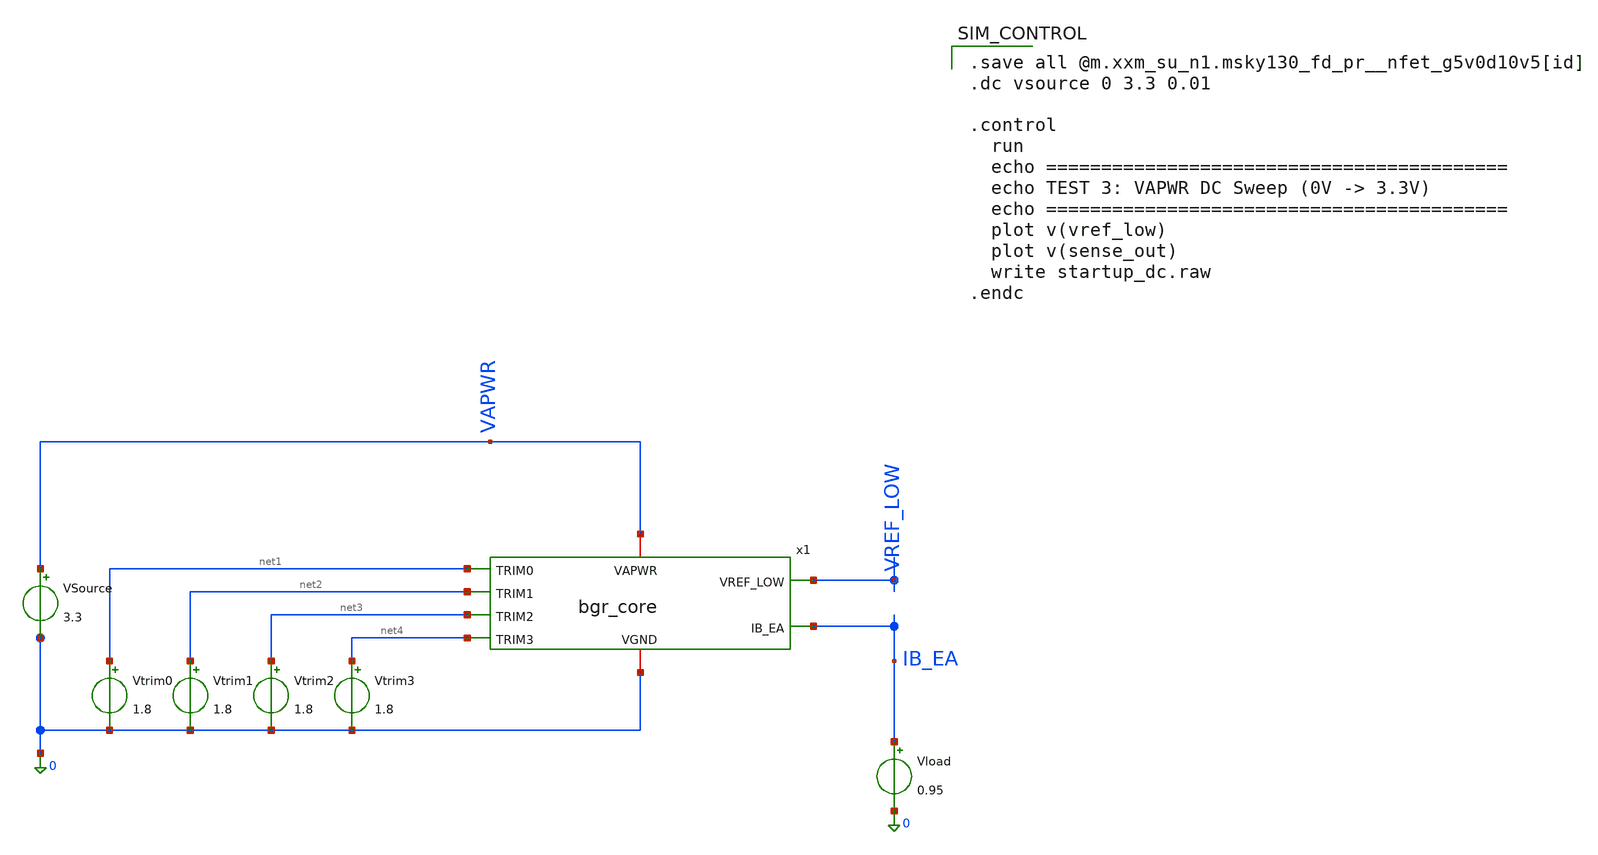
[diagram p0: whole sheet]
** sch_path: designs/bgr_ldo/bgr/bgr_core_tb2.sch
**.subckt bgr_core_tb2
VSource VAPWR 0 3.3
Vload IB_EA 0 0.95
Vtrim0 net1 0 1.8
Vtrim1 net2 0 1.8
Vtrim2 net3 0 1.8
Vtrim3 net4 0 1.8
x1 VAPWR VREF_LOW IB_EA net1 net2 net3 net4 0 bgr_core
**** begin user architecture code

.save all @m.xxm_su_n1.msky130_fd_pr__nfet_g5v0d10v5[id]
.dc vsource 0 3.3 0.01

.control
  run
  echo ==========================================
  echo TEST 3: VAPWR DC Sweep (0V -> 3.3V)
  echo ==========================================
  plot v(vref_low)
  plot v(sense_out)
  write startup_dc.raw
.endc


** opencircuitdesign pdks install
.lib $::SKYWATER_MODELS/sky130.lib.spice tt

**** end user architecture code
**.ends

* expanding   symbol:  bgr_core.sym # of pins=8
** sym_path: designs/bgr_ldo/bgr/bgr_core.sym
** sch_path: designs/bgr_ldo/bgr/bgr_core.sch
.subckt bgr_core VAPWR VREF_LOW IB_EA TRIM0 TRIM1 TRIM2 TRIM3 VGND
*.iopin VAPWR
*.opin VREF_LOW
*.iopin VGND
*.opin IB_EA
*.ipin TRIM0
*.ipin TRIM1
*.ipin TRIM2
*.ipin TRIM3
XXQA VGND VGND VBE1 sky130_fd_pr__pnp_05v5_W0p68L0p68 m=1
XXQB VGND VGND VBE8 sky130_fd_pr__pnp_05v5_W0p68L0p68 m=8
XXM_top1 net2 V_gate_top VAPWR VAPWR sky130_fd_pr__pfet_g5v0d10v5 L=4 W=20 nf=1 ad='int((1 + 1)/2) * 20 / 1 * 0.29'
+ as='int((1 + 2)/2) * 20 / 1 * 0.29' pd='2*int((1 + 1)/2) * (20 / 1 + 0.29)' ps='2*int((1 + 2)/2) * (20 / 1 + 0.29)'
+ nrd='0.29 / 20 ' nrs='0.29 / 20 ' sa=0 sb=0 sd=0 mult=4 m=4
XXM_top2 net3 V_gate_top VAPWR VAPWR sky130_fd_pr__pfet_g5v0d10v5 L=4 W=20 nf=1 ad='int((1 + 1)/2) * 20 / 1 * 0.29'
+ as='int((1 + 2)/2) * 20 / 1 * 0.29' pd='2*int((1 + 1)/2) * (20 / 1 + 0.29)' ps='2*int((1 + 2)/2) * (20 / 1 + 0.29)'
+ nrd='0.29 / 20 ' nrs='0.29 / 20 ' sa=0 sb=0 sd=0 mult=4 m=4
XXM_top5 net6 V_gate_top VAPWR VAPWR sky130_fd_pr__pfet_g5v0d10v5 L=4 W=20 nf=1 ad='int((1 + 1)/2) * 20 / 1 * 0.29'
+ as='int((1 + 2)/2) * 20 / 1 * 0.29' pd='2*int((1 + 1)/2) * (20 / 1 + 0.29)' ps='2*int((1 + 2)/2) * (20 / 1 + 0.29)'
+ nrd='0.29 / 20 ' nrs='0.29 / 20 ' sa=0 sb=0 sd=0 mult=4 m=4
XXM3 net4 V_mid1 VBE1 VGND sky130_fd_pr__nfet_g5v0d10v5 L=4 W=20 nf=1 ad='int((1 + 1)/2) * 20 / 1 * 0.29'
+ as='int((1 + 2)/2) * 20 / 1 * 0.29' pd='2*int((1 + 1)/2) * (20 / 1 + 0.29)' ps='2*int((1 + 2)/2) * (20 / 1 + 0.29)'
+ nrd='0.29 / 20 ' nrs='0.29 / 20 ' sa=0 sb=0 sd=0 mult=2 m=2
XXM4 net5 V_mid1 net1 VGND sky130_fd_pr__nfet_g5v0d10v5 L=4 W=20 nf=1 ad='int((1 + 1)/2) * 20 / 1 * 0.29'
+ as='int((1 + 2)/2) * 20 / 1 * 0.29' pd='2*int((1 + 1)/2) * (20 / 1 + 0.29)' ps='2*int((1 + 2)/2) * (20 / 1 + 0.29)'
+ nrd='0.29 / 20 ' nrs='0.29 / 20 ' sa=0 sb=0 sd=0 mult=2 m=2
XXM_bot1 V_mid1 V_bias net2 VAPWR sky130_fd_pr__pfet_g5v0d10v5 L=2 W=10 nf=1 ad='int((1 + 1)/2) * 10 / 1 * 0.29'
+ as='int((1 + 2)/2) * 10 / 1 * 0.29' pd='2*int((1 + 1)/2) * (10 / 1 + 0.29)' ps='2*int((1 + 2)/2) * (10 / 1 + 0.29)'
+ nrd='0.29 / 10 ' nrs='0.29 / 10 ' sa=0 sb=0 sd=0 mult=4 m=4
XXM_bot2 V_gate_top V_bias net3 VAPWR sky130_fd_pr__pfet_g5v0d10v5 L=2 W=10 nf=1 ad='int((1 + 1)/2) * 10 / 1 * 0.29'
+ as='int((1 + 2)/2) * 10 / 1 * 0.29' pd='2*int((1 + 1)/2) * (10 / 1 + 0.29)' ps='2*int((1 + 2)/2) * (10 / 1 + 0.29)'
+ nrd='0.29 / 10 ' nrs='0.29 / 10 ' sa=0 sb=0 sd=0 mult=4 m=4
XXM_bot5 VREF_LOW V_bias net6 VAPWR sky130_fd_pr__pfet_g5v0d10v5 L=2 W=10 nf=1 ad='int((1 + 1)/2) * 10 / 1 * 0.29'
+ as='int((1 + 2)/2) * 10 / 1 * 0.29' pd='2*int((1 + 1)/2) * (10 / 1 + 0.29)' ps='2*int((1 + 2)/2) * (10 / 1 + 0.29)'
+ nrd='0.29 / 10 ' nrs='0.29 / 10 ' sa=0 sb=0 sd=0 mult=4 m=4
XXM_bias V_bias V_bias VAPWR VAPWR sky130_fd_pr__pfet_g5v0d10v5 L=4 W=10 nf=1 ad='int((1 + 1)/2) * 10 / 1 * 0.29'
+ as='int((1 + 2)/2) * 10 / 1 * 0.29' pd='2*int((1 + 1)/2) * (10 / 1 + 0.29)' ps='2*int((1 + 2)/2) * (10 / 1 + 0.29)'
+ nrd='0.29 / 10 ' nrs='0.29 / 10 ' sa=0 sb=0 sd=0 mult=1 m=1
XXM_bias_mir V_bias_n V_gate_top VAPWR VAPWR sky130_fd_pr__pfet_g5v0d10v5 L=2 W=10 nf=1 ad='int((1 + 1)/2) * 10 / 1 * 0.29'
+ as='int((1 + 2)/2) * 10 / 1 * 0.29' pd='2*int((1 + 1)/2) * (10 / 1 + 0.29)' ps='2*int((1 + 2)/2) * (10 / 1 + 0.29)'
+ nrd='0.29 / 10 ' nrs='0.29 / 10 ' sa=0 sb=0 sd=0 mult=4 m=4
XXM_bias_n1 V_bias_n V_bias_n VGND VGND sky130_fd_pr__nfet_g5v0d10v5 L=2 W=10 nf=1 ad='int((1 + 1)/2) * 10 / 1 * 0.29'
+ as='int((1 + 2)/2) * 10 / 1 * 0.29' pd='2*int((1 + 1)/2) * (10 / 1 + 0.29)' ps='2*int((1 + 2)/2) * (10 / 1 + 0.29)'
+ nrd='0.29 / 10 ' nrs='0.29 / 10 ' sa=0 sb=0 sd=0 mult=2 m=2
XXM_bias_n2 V_bias V_bias_n VGND VGND sky130_fd_pr__nfet_g5v0d10v5 L=2 W=10 nf=1 ad='int((1 + 1)/2) * 10 / 1 * 0.29'
+ as='int((1 + 2)/2) * 10 / 1 * 0.29' pd='2*int((1 + 1)/2) * (10 / 1 + 0.29)' ps='2*int((1 + 2)/2) * (10 / 1 + 0.29)'
+ nrd='0.29 / 10 ' nrs='0.29 / 10 ' sa=0 sb=0 sd=0 mult=2 m=2
XXM_su_n1 V_gate_top sense_out V_su_mid VGND sky130_fd_pr__nfet_g5v0d10v5 L=2 W=1 nf=1 ad='int((1 + 1)/2) * 1 / 1 * 0.29'
+ as='int((1 + 2)/2) * 1 / 1 * 0.29' pd='2*int((1 + 1)/2) * (1 / 1 + 0.29)' ps='2*int((1 + 2)/2) * (1 / 1 + 0.29)'
+ nrd='0.29 / 1 ' nrs='0.29 / 1 ' sa=0 sb=0 sd=0 mult=1 m=1
XXM_su_n2 V_su_mid V_su_mid VGND VGND sky130_fd_pr__nfet_g5v0d10v5 L=20 W=1 nf=1 ad='int((1 + 1)/2) * 1 / 1 * 0.29'
+ as='int((1 + 2)/2) * 1 / 1 * 0.29' pd='2*int((1 + 1)/2) * (1 / 1 + 0.29)' ps='2*int((1 + 2)/2) * (1 / 1 + 0.29)'
+ nrd='0.29 / 1 ' nrs='0.29 / 1 ' sa=0 sb=0 sd=0 mult=1 m=1
XXM_pd sense_out VBE1 VGND VGND sky130_fd_pr__nfet_g5v0d10v5 L=2 W=12 nf=1 ad='int((1 + 1)/2) * 12 / 1 * 0.29'
+ as='int((1 + 2)/2) * 12 / 1 * 0.29' pd='2*int((1 + 1)/2) * (12 / 1 + 0.29)' ps='2*int((1 + 2)/2) * (12 / 1 + 0.29)'
+ nrd='0.29 / 12 ' nrs='0.29 / 12 ' sa=0 sb=0 sd=0 mult=1 m=1
XXM_su1a sense_out V_bias_n net8 VAPWR sky130_fd_pr__pfet_g5v0d10v5 L=20 W=0.42 nf=1 ad='int((1 + 1)/2) * 0.42 / 1 * 0.29'
+ as='int((1 + 2)/2) * 0.42 / 1 * 0.29' pd='2*int((1 + 1)/2) * (0.42 / 1 + 0.29)' ps='2*int((1 + 2)/2) * (0.42 / 1 + 0.29)'
+ nrd='0.29 / 0.42 ' nrs='0.29 / 0.42 ' sa=0 sb=0 sd=0 mult=1 m=1
XXM_su1b net8 V_bias_n net7 VAPWR sky130_fd_pr__pfet_g5v0d10v5 L=20 W=0.42 nf=1 ad='int((1 + 1)/2) * 0.42 / 1 * 0.29'
+ as='int((1 + 2)/2) * 0.42 / 1 * 0.29' pd='2*int((1 + 1)/2) * (0.42 / 1 + 0.29)' ps='2*int((1 + 2)/2) * (0.42 / 1 + 0.29)'
+ nrd='0.29 / 0.42 ' nrs='0.29 / 0.42 ' sa=0 sb=0 sd=0 mult=1 m=1
XXM_su1c net7 V_bias_n VAPWR VAPWR sky130_fd_pr__pfet_g5v0d10v5 L=20 W=0.42 nf=1 ad='int((1 + 1)/2) * 0.42 / 1 * 0.29'
+ as='int((1 + 2)/2) * 0.42 / 1 * 0.29' pd='2*int((1 + 1)/2) * (0.42 / 1 + 0.29)' ps='2*int((1 + 2)/2) * (0.42 / 1 + 0.29)'
+ nrd='0.29 / 0.42 ' nrs='0.29 / 0.42 ' sa=0 sb=0 sd=0 mult=1 m=1
XR1 VBE8 net1 VGND sky130_fd_pr__res_high_po_0p69 L=34.29 mult=1 m=1
XR6_1 n_r6m VBE1 VGND sky130_fd_pr__res_high_po_0p69 L=121.730 mult=1 m=1
XR7_1 n_r7m net1 VGND sky130_fd_pr__res_high_po_0p69 L=121.730 mult=1 m=1
XR2fix n_b0 VREF_LOW VGND sky130_fd_pr__res_high_po_0p69 L=229.410 mult=1 m=1
XXM3c V_mid1 V_casc_n net4 VGND sky130_fd_pr__nfet_g5v0d10v5 L=2 W=10 nf=1 ad='int((1 + 1)/2) * 10 / 1 * 0.29'
+ as='int((1 + 2)/2) * 10 / 1 * 0.29' pd='2*int((1 + 1)/2) * (10 / 1 + 0.29)' ps='2*int((1 + 2)/2) * (10 / 1 + 0.29)'
+ nrd='0.29 / 10 ' nrs='0.29 / 10 ' sa=0 sb=0 sd=0 mult=2 m=2
XXM4c V_gate_top V_casc_n net5 VGND sky130_fd_pr__nfet_g5v0d10v5 L=2 W=10 nf=1 ad='int((1 + 1)/2) * 10 / 1 * 0.29'
+ as='int((1 + 2)/2) * 10 / 1 * 0.29' pd='2*int((1 + 1)/2) * (10 / 1 + 0.29)' ps='2*int((1 + 2)/2) * (10 / 1 + 0.29)'
+ nrd='0.29 / 10 ' nrs='0.29 / 10 ' sa=0 sb=0 sd=0 mult=2 m=2
XXM_cn_mir V_casc_n V_gate_top VAPWR VAPWR sky130_fd_pr__pfet_g5v0d10v5 L=2 W=10 nf=1 ad='int((1 + 1)/2) * 10 / 1 * 0.29'
+ as='int((1 + 2)/2) * 10 / 1 * 0.29' pd='2*int((1 + 1)/2) * (10 / 1 + 0.29)' ps='2*int((1 + 2)/2) * (10 / 1 + 0.29)'
+ nrd='0.29 / 10 ' nrs='0.29 / 10 ' sa=0 sb=0 sd=0 mult=1 m=1
XXM_cn_d2 V_casc_n V_casc_n cn_mid VGND sky130_fd_pr__nfet_g5v0d10v5 L=2 W=2 nf=1 ad='int((1 + 1)/2) * 2 / 1 * 0.29'
+ as='int((1 + 2)/2) * 2 / 1 * 0.29' pd='2*int((1 + 1)/2) * (2 / 1 + 0.29)' ps='2*int((1 + 2)/2) * (2 / 1 + 0.29)'
+ nrd='0.29 / 2 ' nrs='0.29 / 2 ' sa=0 sb=0 sd=0 mult=1 m=1
XXM_cn_d1 cn_mid cn_mid net9 VGND sky130_fd_pr__nfet_g5v0d10v5 L=2 W=2 nf=1 ad='int((1 + 1)/2) * 2 / 1 * 0.29'
+ as='int((1 + 2)/2) * 2 / 1 * 0.29' pd='2*int((1 + 1)/2) * (2 / 1 + 0.29)' ps='2*int((1 + 2)/2) * (2 / 1 + 0.29)'
+ nrd='0.29 / 2 ' nrs='0.29 / 2 ' sa=0 sb=0 sd=0 mult=1 m=1
XR_cn VGND net9 VGND sky130_fd_pr__res_high_po_0p69 L=91.205 mult=1 m=1
XXM_tap_top net_tap V_gate_top VAPWR VAPWR sky130_fd_pr__pfet_g5v0d10v5 L=4 W=20 nf=1 ad='int((1 + 1)/2) * 20 / 1 * 0.29'
+ as='int((1 + 2)/2) * 20 / 1 * 0.29' pd='2*int((1 + 1)/2) * (20 / 1 + 0.29)' ps='2*int((1 + 2)/2) * (20 / 1 + 0.29)'
+ nrd='0.29 / 20 ' nrs='0.29 / 20 ' sa=0 sb=0 sd=0 mult=1 m=1
XXM_tap_casc IB_EA V_bias net_tap VAPWR sky130_fd_pr__pfet_g5v0d10v5 L=2 W=10 nf=1 ad='int((1 + 1)/2) * 10 / 1 * 0.29'
+ as='int((1 + 2)/2) * 10 / 1 * 0.29' pd='2*int((1 + 1)/2) * (10 / 1 + 0.29)' ps='2*int((1 + 2)/2) * (10 / 1 + 0.29)'
+ nrd='0.29 / 10 ' nrs='0.29 / 10 ' sa=0 sb=0 sd=0 mult=1 m=1
XR2b0 n_b1 n_b0 VGND sky130_fd_pr__res_high_po_0p69 L=1.27 mult=1 m=1
XR2b1 n_b2 n_b1 VGND sky130_fd_pr__res_high_po_0p69 L=3.650 mult=1 m=1
XR2b2 n_b3 n_b2 VGND sky130_fd_pr__res_high_po_0p69 L=8.42 mult=1 m=1
XR2b3 VGND n_b3 VGND sky130_fd_pr__res_high_po_0p69 L=17.96 mult=1 m=1
x1 VGND n_b1 n_b0 n_b3 n_b2 TRIM0 TRIM1 TRIM3 TRIM2 VGND n_b3 n_b2 n_b1 trim_sw
XR6_2 VGND n_r6m VGND sky130_fd_pr__res_high_po_0p69 L=121.730 mult=1 m=1
XR7_2 VGND n_r7m VGND sky130_fd_pr__res_high_po_0p69 L=121.730 mult=1 m=1
XXDUM_B1 VAPWR VAPWR VAPWR VAPWR sky130_fd_pr__pfet_g5v0d10v5 L=2 W=10 nf=1 ad='int((1 + 1)/2) * 10 / 1 * 0.29'
+ as='int((1 + 2)/2) * 10 / 1 * 0.29' pd='2*int((1 + 1)/2) * (10 / 1 + 0.29)' ps='2*int((1 + 2)/2) * (10 / 1 + 0.29)'
+ nrd='0.29 / 10 ' nrs='0.29 / 10 ' sa=0 sb=0 sd=0 mult=1 m=1
XXDUM_B2 VAPWR VAPWR VAPWR VAPWR sky130_fd_pr__pfet_g5v0d10v5 L=2 W=10 nf=1 ad='int((1 + 1)/2) * 10 / 1 * 0.29'
+ as='int((1 + 2)/2) * 10 / 1 * 0.29' pd='2*int((1 + 1)/2) * (10 / 1 + 0.29)' ps='2*int((1 + 2)/2) * (10 / 1 + 0.29)'
+ nrd='0.29 / 10 ' nrs='0.29 / 10 ' sa=0 sb=0 sd=0 mult=1 m=1
XXDUM_C1 VGND VGND VGND VGND sky130_fd_pr__nfet_g5v0d10v5 L=4 W=20 nf=1 ad='int((1 + 1)/2) * 20 / 1 * 0.29'
+ as='int((1 + 2)/2) * 20 / 1 * 0.29' pd='2*int((1 + 1)/2) * (20 / 1 + 0.29)' ps='2*int((1 + 2)/2) * (20 / 1 + 0.29)'
+ nrd='0.29 / 20 ' nrs='0.29 / 20 ' sa=0 sb=0 sd=0 mult=1 m=1
XXDUM_C2 VGND VGND VGND VGND sky130_fd_pr__nfet_g5v0d10v5 L=4 W=20 nf=1 ad='int((1 + 1)/2) * 20 / 1 * 0.29'
+ as='int((1 + 2)/2) * 20 / 1 * 0.29' pd='2*int((1 + 1)/2) * (20 / 1 + 0.29)' ps='2*int((1 + 2)/2) * (20 / 1 + 0.29)'
+ nrd='0.29 / 20 ' nrs='0.29 / 20 ' sa=0 sb=0 sd=0 mult=1 m=1
XXDUM_D1 VGND VGND VGND VGND sky130_fd_pr__nfet_g5v0d10v5 L=2 W=10 nf=1 ad='int((1 + 1)/2) * 10 / 1 * 0.29'
+ as='int((1 + 2)/2) * 10 / 1 * 0.29' pd='2*int((1 + 1)/2) * (10 / 1 + 0.29)' ps='2*int((1 + 2)/2) * (10 / 1 + 0.29)'
+ nrd='0.29 / 10 ' nrs='0.29 / 10 ' sa=0 sb=0 sd=0 mult=1 m=1
XXDUM_D2 VGND VGND VGND VGND sky130_fd_pr__nfet_g5v0d10v5 L=2 W=10 nf=1 ad='int((1 + 1)/2) * 10 / 1 * 0.29'
+ as='int((1 + 2)/2) * 10 / 1 * 0.29' pd='2*int((1 + 1)/2) * (10 / 1 + 0.29)' ps='2*int((1 + 2)/2) * (10 / 1 + 0.29)'
+ nrd='0.29 / 10 ' nrs='0.29 / 10 ' sa=0 sb=0 sd=0 mult=1 m=1
XXDUM_Qn VGND VGND VGND sky130_fd_pr__pnp_05v5_W0p68L0p68 m=16
XXDUM_RA1 VGND VGND VGND sky130_fd_pr__res_high_po_0p69 L=31.49 mult=1 m=1
XXDUM_RA2 VGND VGND VGND sky130_fd_pr__res_high_po_0p69 L=31.49 mult=1 m=1
XXDUM_RB1 VGND VGND VGND sky130_fd_pr__res_high_po_0p69 L=58.41 mult=1 m=1
XXDUM_RB2 VGND VGND VGND sky130_fd_pr__res_high_po_0p69 L=58.41 mult=1 m=1
.ends


* expanding   symbol:  trim_sw.sym # of pins=13
** sym_path: designs/bgr_ldo/bgr/trim_sw.sym
** sch_path: designs/bgr_ldo/bgr/trim_sw.sch
.subckt trim_sw VGND SEG1A SEG0A SEG3A SEG2A TRIM0 TRIM1 TRIM3 TRIM2 SEG3B SEG2B SEG1B SEG0B
*.ipin TRIM0
*.ipin TRIM1
*.ipin TRIM2
*.ipin TRIM3
*.iopin SEG0A
*.iopin SEG0B
*.iopin SEG1A
*.iopin SEG2A
*.iopin SEG3A
*.iopin SEG1B
*.iopin SEG2B
*.iopin SEG3B
*.iopin VGND
XSWb0 SEG0A TRIM0 SEG0B VGND sky130_fd_pr__nfet_01v8 L=0.15 W=10 nf=1 ad='int((1 + 1)/2) * 10 / 1 * 0.29'
+ as='int((1 + 2)/2) * 10 / 1 * 0.29' pd='2*int((1 + 1)/2) * (10 / 1 + 0.29)' ps='2*int((1 + 2)/2) * (10 / 1 + 0.29)'
+ nrd='0.29 / 10 ' nrs='0.29 / 10 ' sa=0 sb=0 sd=0 mult=22 m=22
XSWb1 SEG1A TRIM1 SEG1B VGND sky130_fd_pr__nfet_01v8 L=0.15 W=10 nf=1 ad='int((1 + 1)/2) * 10 / 1 * 0.29'
+ as='int((1 + 2)/2) * 10 / 1 * 0.29' pd='2*int((1 + 1)/2) * (10 / 1 + 0.29)' ps='2*int((1 + 2)/2) * (10 / 1 + 0.29)'
+ nrd='0.29 / 10 ' nrs='0.29 / 10 ' sa=0 sb=0 sd=0 mult=22 m=22
XSWb2 SEG2A TRIM2 SEG2B VGND sky130_fd_pr__nfet_01v8 L=0.15 W=10 nf=1 ad='int((1 + 1)/2) * 10 / 1 * 0.29'
+ as='int((1 + 2)/2) * 10 / 1 * 0.29' pd='2*int((1 + 1)/2) * (10 / 1 + 0.29)' ps='2*int((1 + 2)/2) * (10 / 1 + 0.29)'
+ nrd='0.29 / 10 ' nrs='0.29 / 10 ' sa=0 sb=0 sd=0 mult=22 m=22
XSWb3 SEG3A TRIM3 SEG3B VGND sky130_fd_pr__nfet_01v8 L=0.15 W=10 nf=1 ad='int((1 + 1)/2) * 10 / 1 * 0.29'
+ as='int((1 + 2)/2) * 10 / 1 * 0.29' pd='2*int((1 + 1)/2) * (10 / 1 + 0.29)' ps='2*int((1 + 2)/2) * (10 / 1 + 0.29)'
+ nrd='0.29 / 10 ' nrs='0.29 / 10 ' sa=0 sb=0 sd=0 mult=22 m=22
.ends

.end
